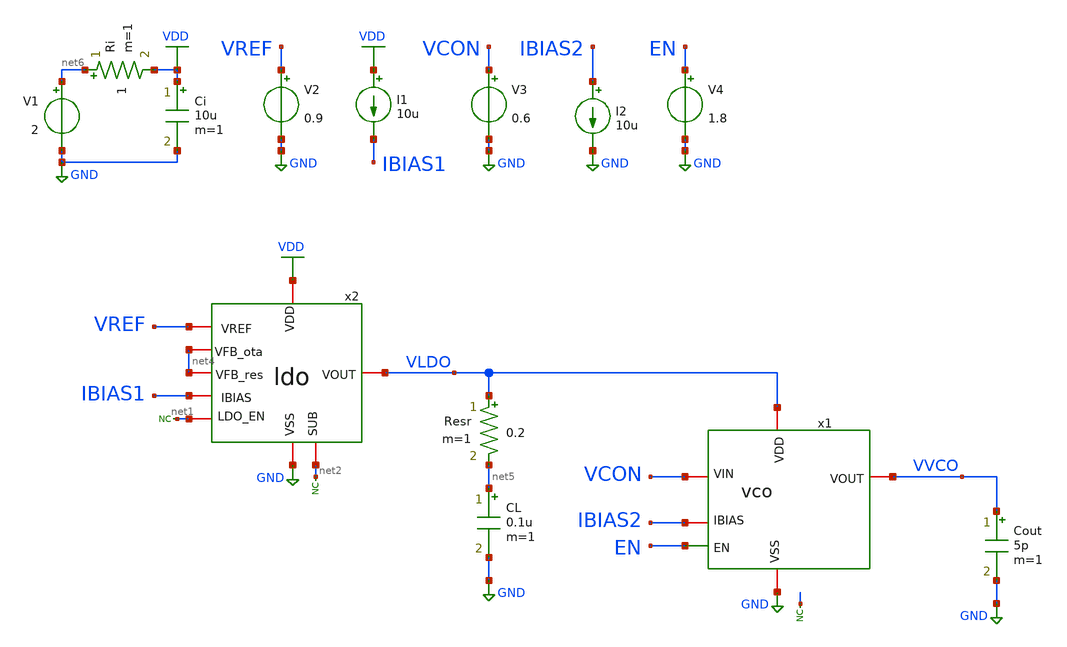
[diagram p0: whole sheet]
** sch_path: designs/libs/tb_top/tb_top/tb_top_ldo_vco_dc/tb_top_ldo_vco_dc.sch
**.subckt tb_top_ldo_vco_dc
V3 VCON GND 0.6
I2 IBIAS2 GND 10u
V4 EN GND 1.8
x1 VLDO IBIAS2 VVCO EN GND VCON vco
x2 VDD VREF VLDO IBIAS1 net2 GND net1 net4 net4 ldo
* noconn #net1
* noconn #net2
* noconn #net3
V2 VREF GND 0.9
CL net5 GND 0.1u m=1
Resr VLDO net5 0.2 m=1
I1 VDD IBIAS1 10u
Ri net6 VDD 1 m=1
Ci VDD GND 10u m=1
V1 net6 GND 2
Cout VVCO GND 5p m=1
**** begin user architecture code



.control
save all

run
set color0 = white

** SIMULATIONS
dc V1 2 5 0.01

** PLOTS
setplot dc1
let vldo = v(VLDO)
plot vldo

** MEASUREMENTS
meas dc Vldo_max MAX v(VLDO)
meas dc Vldo_min MIN v(VLDO)

write tb_top_ldo_vco_dc.raw

.endc
* ngspice commands




.include $::180MCU_MODELS/design.ngspice
.lib $::180MCU_MODELS/sm141064.ngspice typical
.lib $::180MCU_MODELS/sm141064.ngspice cap_mim
.lib $::180MCU_MODELS/sm141064.ngspice moscap_typical
.lib $::180MCU_MODELS/sm141064.ngspice mimcap_typical
.lib $::180MCU_MODELS/sm141064.ngspice res_typical
* .lib $::180MCU_MODELS/sm141064.ngspice res_statistical
* ngspice commands

**** end user architecture code
**.ends
.GLOBAL VDD
.GLOBAL GND
.end
